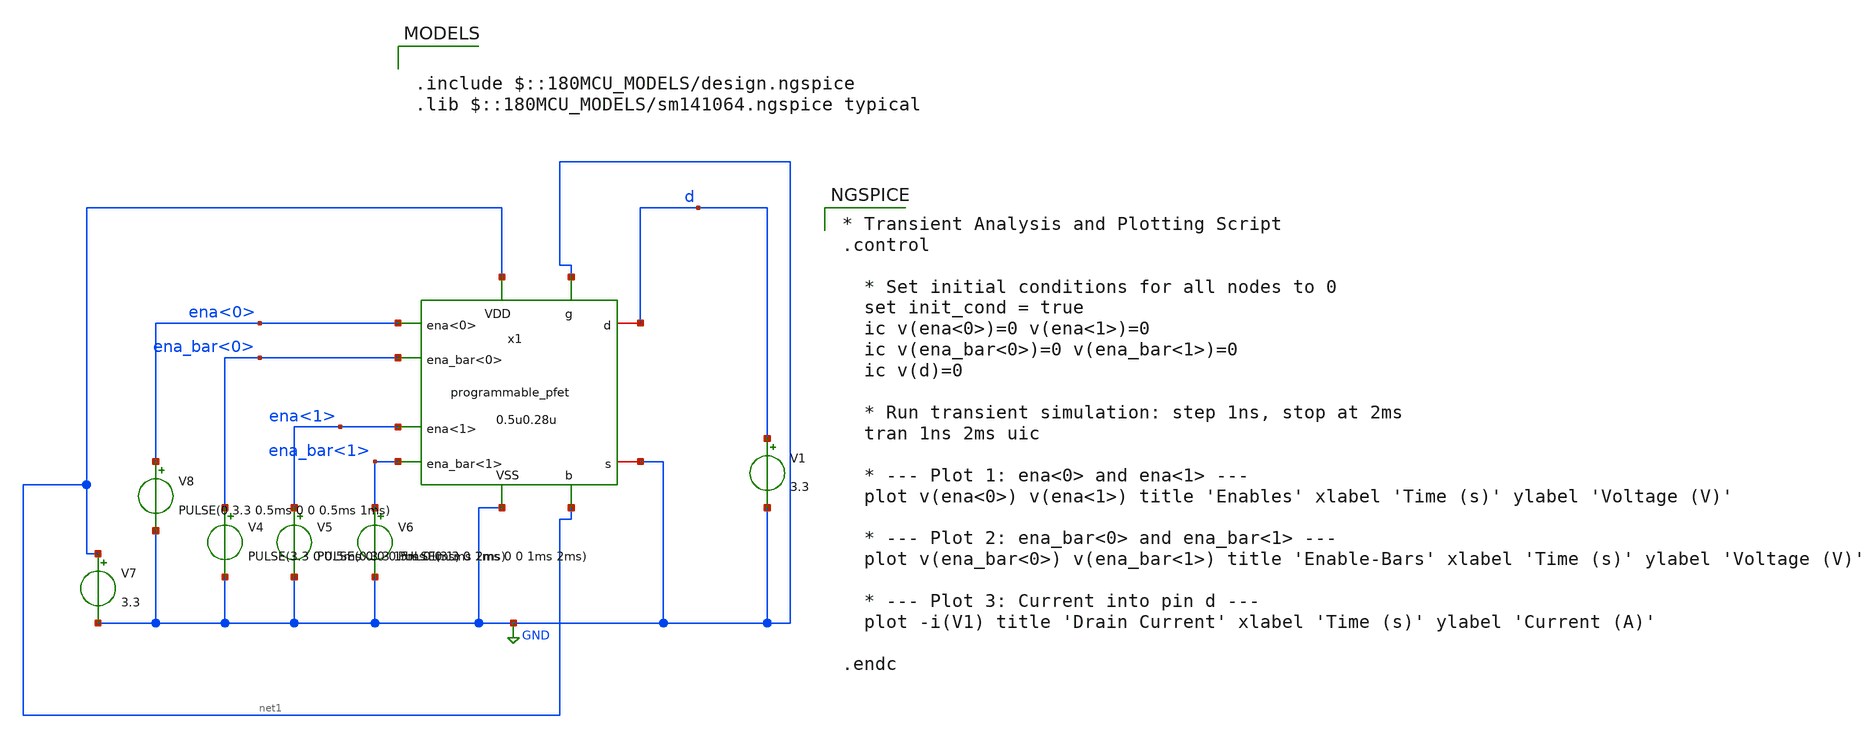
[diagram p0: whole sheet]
** sch_path: designs/libs/core_digital/TB_prog_fet.sch
**.subckt TB_prog_fet
V4 ena_bar<0> GND PULSE(3.3 0 0.5ms 0 0 0.5ms 1ms)
V5 ena<1> GND PULSE(0 3.3 1ms 0 0 1ms 2ms)
V6 ena_bar<1> GND PULSE(3.3 0 1ms 0 0 1ms 2ms)
V7 net1 GND 3.3
V8 ena<0> GND PULSE(0 3.3 0.5ms 0 0 0.5ms 1ms)
V1 d GND 3.3
x1 d net1 GND GND ena_bar<0> net1 ena_bar<1> ena<0> ena<1> GND programmable_pfet width=0.5u
+ length=0.28u
**** begin user architecture code

.include $::180MCU_MODELS/design.ngspice
.lib $::180MCU_MODELS/sm141064.ngspice typical


* Transient Analysis and Plotting Script
.control

  * Set initial conditions for all nodes to 0
  set init_cond = true
  ic v(ena<0>)=0 v(ena<1>)=0
  ic v(ena_bar<0>)=0 v(ena_bar<1>)=0
  ic v(d)=0

  * Run transient simulation: step 1ns, stop at 2ms
  tran 1ns 2ms uic

  * --- Plot 1: ena<0> and ena<1> ---
  plot v(ena<0>) v(ena<1>) title 'Enables' xlabel 'Time (s)' ylabel 'Voltage (V)'

  * --- Plot 2: ena_bar<0> and ena_bar<1> ---
  plot v(ena_bar<0>) v(ena_bar<1>) title 'Enable-Bars' xlabel 'Time (s)' ylabel 'Voltage (V)'

  * --- Plot 3: Current into pin d ---
  plot -i(V1) title 'Drain Current' xlabel 'Time (s)' ylabel 'Current (A)'

.endc

**** end user architecture code
**.ends

* expanding   symbol:  libs/core_digital/programmable_pfet.sym # of pins=10
** sym_path: designs/libs/core_digital/programmable_pfet.sym
** sch_path: designs/libs/core_digital/programmable_pfet.sch
.subckt programmable_pfet d b g s ena_bar<0> VDD ena_bar<1> ena<0> ena<1> VSS  width=0.22u
+ length=0.28u
*.ipin VSS
*.ipin VDD
*.ipin g
*.ipin ena_bar<1>
*.ipin ena_bar<0>
*.ipin ena<0>
*.iopin d
*.iopin s
*.ipin b
*.ipin ena<1>
x1 ena_bar<0> VDD net2 g VSS ena<0> transmission_gate
x3 ena_bar<1> VDD net1 g VSS ena<1> transmission_gate
XM1 s net2 d b pfet_03v3 L={length} W={width} nf=1 ad='int((nf+1)/2) * W/nf * 0.18u' as='int((nf+2)/2) * W/nf * 0.18u'
+ pd='2*int((nf+1)/2) * (W/nf + 0.18u)' ps='2*int((nf+2)/2) * (W/nf + 0.18u)' nrd='0.18u / W' nrs='0.18u / W'
+ sa=0 sb=0 sd=0 m=1
XM3 s net1 d b pfet_03v3 L={length} W={2*width} nf=1 ad='int((nf+1)/2) * W/nf * 0.18u' as='int((nf+2)/2) * W/nf * 0.18u'
+ pd='2*int((nf+1)/2) * (W/nf + 0.18u)' ps='2*int((nf+2)/2) * (W/nf + 0.18u)' nrd='0.18u / W' nrs='0.18u / W'
+ sa=0 sb=0 sd=0 m=1
XM2 net1 ena_bar<1> VDD VDD pfet_03v3 L=0.28u W=0.22u nf=1 ad='int((nf+1)/2) * W/nf * 0.18u' as='int((nf+2)/2) * W/nf * 0.18u'
+ pd='2*int((nf+1)/2) * (W/nf + 0.18u)' ps='2*int((nf+2)/2) * (W/nf + 0.18u)' nrd='0.18u / W' nrs='0.18u / W'
+ sa=0 sb=0 sd=0 m=1
XM4 net2 ena_bar<0> VDD VDD pfet_03v3 L=0.28u W=0.22u nf=1 ad='int((nf+1)/2) * W/nf * 0.18u' as='int((nf+2)/2) * W/nf * 0.18u'
+ pd='2*int((nf+1)/2) * (W/nf + 0.18u)' ps='2*int((nf+2)/2) * (W/nf + 0.18u)' nrd='0.18u / W' nrs='0.18u / W'
+ sa=0 sb=0 sd=0 m=1
.ends


* expanding   symbol:  libs/core_digital/transmission_gate.sym # of pins=6
** sym_path: designs/libs/core_digital/schem/transmission_gate.sym
** sch_path: designs/libs/core_digital/schem/transmission_gate.sch
.subckt transmission_gate ena_bar VDD out in VSS ena
*.ipin in
*.ipin ena_bar
*.ipin ena
*.ipin VSS
*.ipin VDD
*.opin out
XM1 in ena_bar out VDD pfet_03v3 L=0.28u W=0.22u nf=1 ad='int((nf+1)/2) * W/nf * 0.18u' as='int((nf+2)/2) * W/nf * 0.18u'
+ pd='2*int((nf+1)/2) * (W/nf + 0.18u)' ps='2*int((nf+2)/2) * (W/nf + 0.18u)' nrd='0.18u / W' nrs='0.18u / W'
+ sa=0 sb=0 sd=0 m=1
XM2 in ena out VSS nfet_03v3 L=0.28u W=0.22u nf=1 ad='int((nf+1)/2) * W/nf * 0.18u' as='int((nf+2)/2) * W/nf * 0.18u'
+ pd='2*int((nf+1)/2) * (W/nf + 0.18u)' ps='2*int((nf+2)/2) * (W/nf + 0.18u)' nrd='0.18u / W' nrs='0.18u / W'
+ sa=0 sb=0 sd=0 m=1
.ends

.GLOBAL GND
.end
